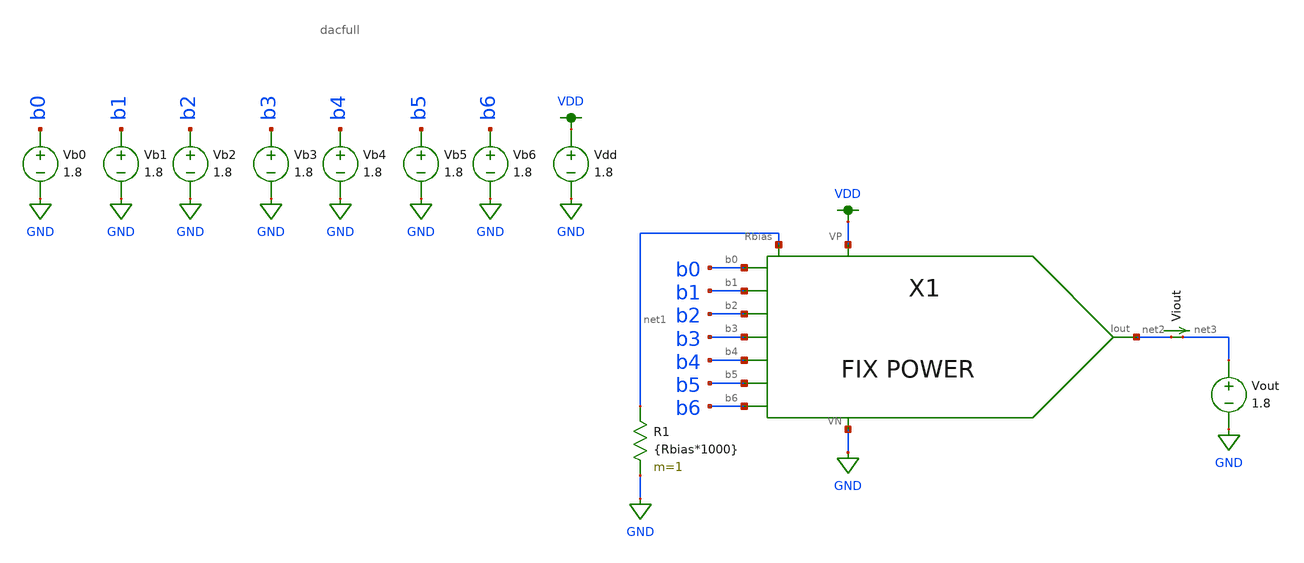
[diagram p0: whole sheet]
** sch_path: design-files/opt/dac_harness_fixed_opt.sch
**.subckt dac_harness_fixed_opt
X1 VDD b0 b1 b2 b3 b4 b5 b6 GND net2 net1 dacfull
Vb0 b0 GND 1.8
Vb1 b1 GND 1.8
Vb2 b2 GND 1.8
Vb3 b3 GND 1.8
Vb4 b4 GND 1.8
Vb5 b5 GND 1.8
Vb6 b6 GND 1.8
Vdd VDD GND 1.8
R1 net1 GND {Rbias*1000} m=1
Viout net2 net3 0
.save i(viout)
Vout net3 GND 1.8
**** begin user architecture code


.param llen=1.4
.param lwid=5.7
.param blen=0.5
.param bwid=1.4
.param brlen=0.3
.param brwid=3.15
.param Rbias=250
.control
set wr_vecnames
set wr_singlescale
dc Vout 0 1.8 0.01
save i(Viout)
wrdata ~/VLSI/VLSI-MP4/design-files/opt/dacdata_fixed.txt i(Viout)
quit
.endc



.option wnflag=1
.param MC_SWITCH=0
.lib ~/skywater/skywater-pdk/libraries/sky130_fd_pr_ngspice/latest/models/sky130.lib.spice tt

**** end user architecture code
**.ends
.GLOBAL GND
.GLOBAL VDD
.end
